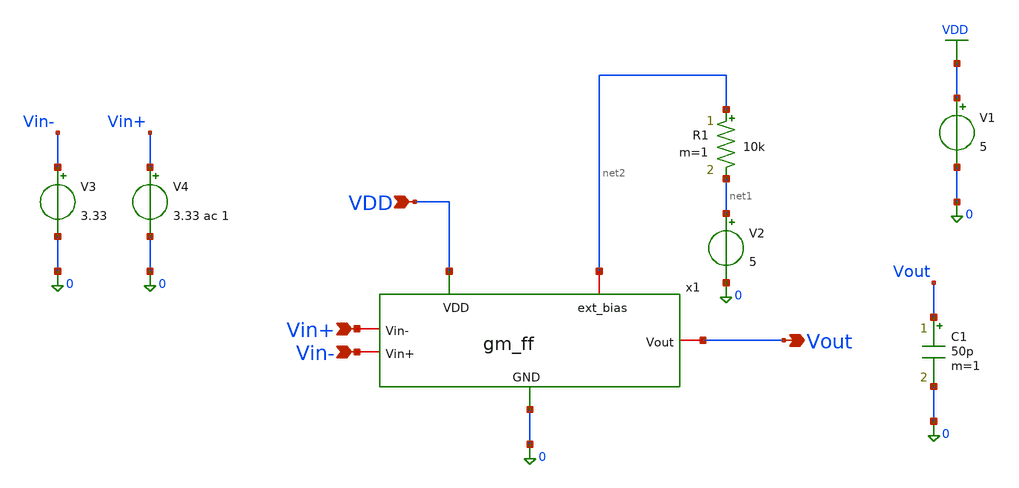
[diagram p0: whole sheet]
** sch_path: TG_gm_ff/gm_ff_testing.sch
**.subckt gm_ff_testing VDD Vin- Vin+ Vout
*.ipin VDD
*.ipin Vin-
*.ipin Vin+
*.opin Vout
V1 VDD 0 5
V3 Vin- 0 3.33
V4 Vin+ 0 3.33 ac 1
R1 net2 net1 10k m=1
V2 net1 0 5
C1 Vout 0 50p m=1
x1 VDD Vout Vin+ Vin- net2 0 gm_ff
**** begin user architecture code



.include /foss/pdks/gf180mcuD/libs.tech/ngspice/design.ngspice
.lib /foss/pdks/gf180mcuD/libs.tech/ngspice/sm141064.ngspice typical
.lib /foss/pdks/gf180mcuD/libs.tech/ngspice/sm141064.ngspice res_typical
.lib /foss/pdks/gf180mcuD/libs.tech/ngspice/sm141064.ngspice moscap_typical
.lib /foss/pdks/gf180mcuD/libs.tech/ngspice/sm141064.ngspice mimcap_typical
.lib /foss/pdks/gf180mcuD/libs.tech/ngspice/sm141064.ngspice cap_mim


.control
  save all
  op
  print all
  *print @m.xm2.m0[gm]
  *print @m.xm2.m0[id]
  *show all
  ac dec 10 1 1G
  meas ac dc_gain MAX vdb(Vout)
  meas ac ugbw WHEN vdb(Vout)=0 FALL=1
  let phase_deg = (180/PI)*vp(Vout)
  plot vdb(Vout)
  plot phase_deg
.endc



**** end user architecture code
**.ends

* expanding   symbol:  TG_gm_ff/gm_ff.sym # of pins=6
** sym_path: MRTMOS_final_chip/gm_ff.sym
** sch_path: MRTMOS_final_chip/gm_ff.sch
.subckt gm_ff VDD Vout Vin- Vin+ ext_bias GND
*.iopin ext_bias
*.ipin Vin+
*.ipin Vin-
*.iopin GND
*.iopin VDD
*.opin Vout
XC3 ext_bias GND cap_nmos_06v0 c_width=60e-6 c_length=10e-6 m=6
XC1 VDD GND cap_nmos_06v0 c_width=60e-6 c_length=10e-6 m=6
XM7 net2 ext_bias GND GND nfet_05v0 L=1.2u W=16u nf=8 ad='int((nf+1)/2) * W/nf * 0.18u' as='int((nf+2)/2) * W/nf * 0.18u'
+ pd='2*int((nf+1)/2) * (W/nf + 0.18u)' ps='2*int((nf+2)/2) * (W/nf + 0.18u)' nrd='0.18u / W' nrs='0.18u / W'
+ sa=0 sb=0 sd=0 m=2
XM8 Vout Vin- net2 GND nfet_05v0 L=1u W=7.5u nf=4 ad='int((nf+1)/2) * W/nf * 0.18u' as='int((nf+2)/2) * W/nf * 0.18u'
+ pd='2*int((nf+1)/2) * (W/nf + 0.18u)' ps='2*int((nf+2)/2) * (W/nf + 0.18u)' nrd='0.18u / W' nrs='0.18u / W'
+ sa=0 sb=0 sd=0 m=4
XM9 net1 net1 VDD VDD pfet_05v0 L=2u W=17u nf=10 ad='int((nf+1)/2) * W/nf * 0.18u' as='int((nf+2)/2) * W/nf * 0.18u'
+ pd='2*int((nf+1)/2) * (W/nf + 0.18u)' ps='2*int((nf+2)/2) * (W/nf + 0.18u)' nrd='0.18u / W' nrs='0.18u / W'
+ sa=0 sb=0 sd=0 m=2
XM5 ext_bias ext_bias GND GND nfet_05v0 L=1.2u W=16u nf=8 ad='int((nf+1)/2) * W/nf * 0.18u' as='int((nf+2)/2) * W/nf * 0.18u'
+ pd='2*int((nf+1)/2) * (W/nf + 0.18u)' ps='2*int((nf+2)/2) * (W/nf + 0.18u)' nrd='0.18u / W' nrs='0.18u / W'
+ sa=0 sb=0 sd=0 m=2
XM1 net1 Vin+ net2 GND nfet_05v0 L=1u W=7.5u nf=4 ad='int((nf+1)/2) * W/nf * 0.18u' as='int((nf+2)/2) * W/nf * 0.18u'
+ pd='2*int((nf+1)/2) * (W/nf + 0.18u)' ps='2*int((nf+2)/2) * (W/nf + 0.18u)' nrd='0.18u / W' nrs='0.18u / W'
+ sa=0 sb=0 sd=0 m=4
XM2 Vout net1 VDD VDD pfet_05v0 L=2u W=17u nf=10 ad='int((nf+1)/2) * W/nf * 0.18u' as='int((nf+2)/2) * W/nf * 0.18u'
+ pd='2*int((nf+1)/2) * (W/nf + 0.18u)' ps='2*int((nf+2)/2) * (W/nf + 0.18u)' nrd='0.18u / W' nrs='0.18u / W'
+ sa=0 sb=0 sd=0 m=2
.ends

.GLOBAL VDD
.end
